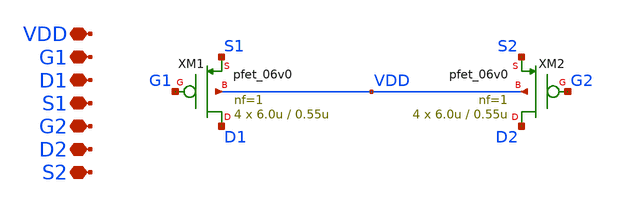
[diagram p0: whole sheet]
** sch_path: designs/libs/core_single-fet/pfet-vdd/pfet-vdd.sch
**.subckt pfet-vdd VDD S1 G1 D1 S2 G2 D2
*.iopin VDD
*.iopin S1
*.iopin G1
*.iopin D1
*.iopin S2
*.iopin G2
*.iopin D2
XM1 D1 G1 S1 VDD pfet_06v0 L=0.55u W=6.0u nf=1 ad='int((nf+1)/2) * W/nf * 0.18u' as='int((nf+2)/2) * W/nf * 0.18u'
+ pd='2*int((nf+1)/2) * (W/nf + 0.18u)' ps='2*int((nf+2)/2) * (W/nf + 0.18u)' nrd='0.18u / W' nrs='0.18u / W'
+ sa=0 sb=0 sd=0 m=4
XM2 D2 G2 S2 VDD pfet_06v0 L=0.55u W=6.0u nf=1 ad='int((nf+1)/2) * W/nf * 0.18u' as='int((nf+2)/2) * W/nf * 0.18u'
+ pd='2*int((nf+1)/2) * (W/nf + 0.18u)' ps='2*int((nf+2)/2) * (W/nf + 0.18u)' nrd='0.18u / W' nrs='0.18u / W'
+ sa=0 sb=0 sd=0 m=4
**.ends
.end
